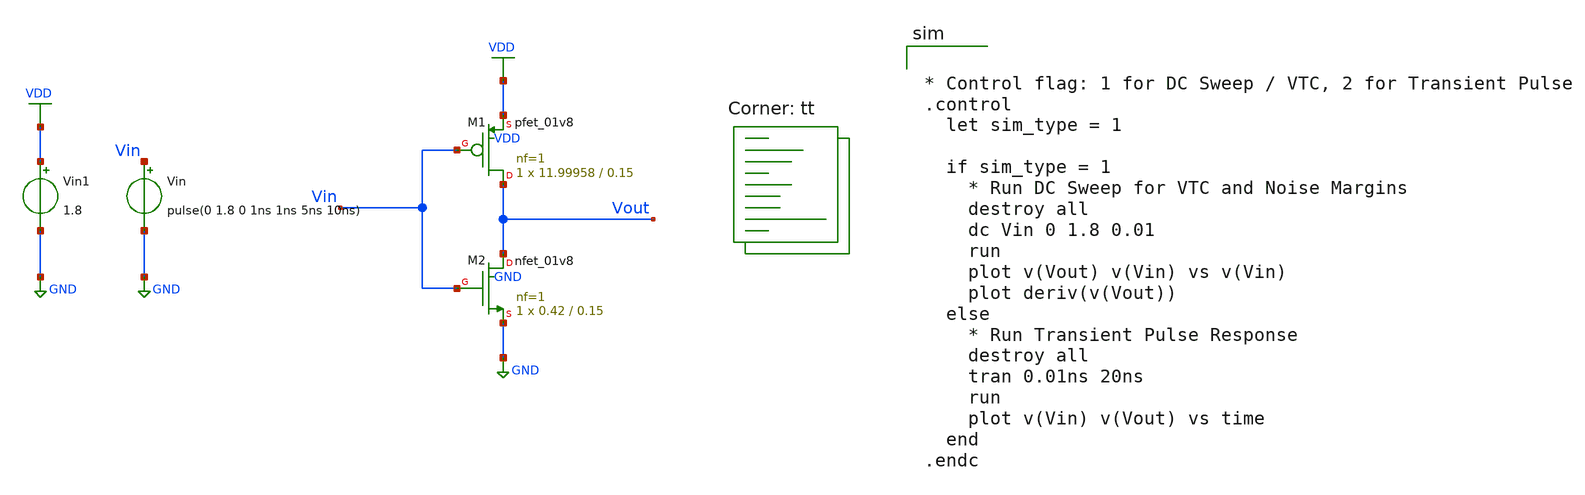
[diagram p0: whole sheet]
** sch_path: assignments/assignment2/assign1b.sch
**.subckt assign1b
Vin Vin GND pulse(0 1.8 0 1ns 1ns 5ns 10ns)
XM1 Vout Vin VDD VDD sky130_fd_pr__pfet_01v8 L=0.15 W=11.99958 nf=1 ad='int((nf+1)/2) * W/nf * 0.29'
+ as='int((nf+2)/2) * W/nf * 0.29' pd='2*int((nf+1)/2) * (W/nf + 0.29)' ps='2*int((nf+2)/2) * (W/nf + 0.29)'
+ nrd='0.29 / W' nrs='0.29 / W' sa=0 sb=0 sd=0 mult=1 m=1
XM2 Vout Vin GND GND sky130_fd_pr__nfet_01v8 L=0.15 W=0.42 nf=1 ad='int((nf+1)/2) * W/nf * 0.29' as='int((nf+2)/2) * W/nf * 0.29'
+ pd='2*int((nf+1)/2) * (W/nf + 0.29)' ps='2*int((nf+2)/2) * (W/nf + 0.29)' nrd='0.29 / W' nrs='0.29 / W'
+ sa=0 sb=0 sd=0 mult=1 m=1
Vin1 VDD GND 1.8
**** begin user architecture code


* Control flag: 1 for DC Sweep / VTC, 2 for Transient Pulse
.control
  let sim_type = 1

  if sim_type = 1
    * Run DC Sweep for VTC and Noise Margins
    destroy all
    dc Vin 0 1.8 0.01
    run
    plot v(Vout) v(Vin) vs v(Vin)
    plot deriv(v(Vout))
  else
    * Run Transient Pulse Response
    destroy all
    tran 0.01ns 20ns
    run
    plot v(Vin) v(Vout) vs time
  end
.endc


.lib $::SKYWATER_MODELS/sky130.lib.spice tt
**** end user architecture code
**.ends
.GLOBAL GND
.GLOBAL VDD
.end
